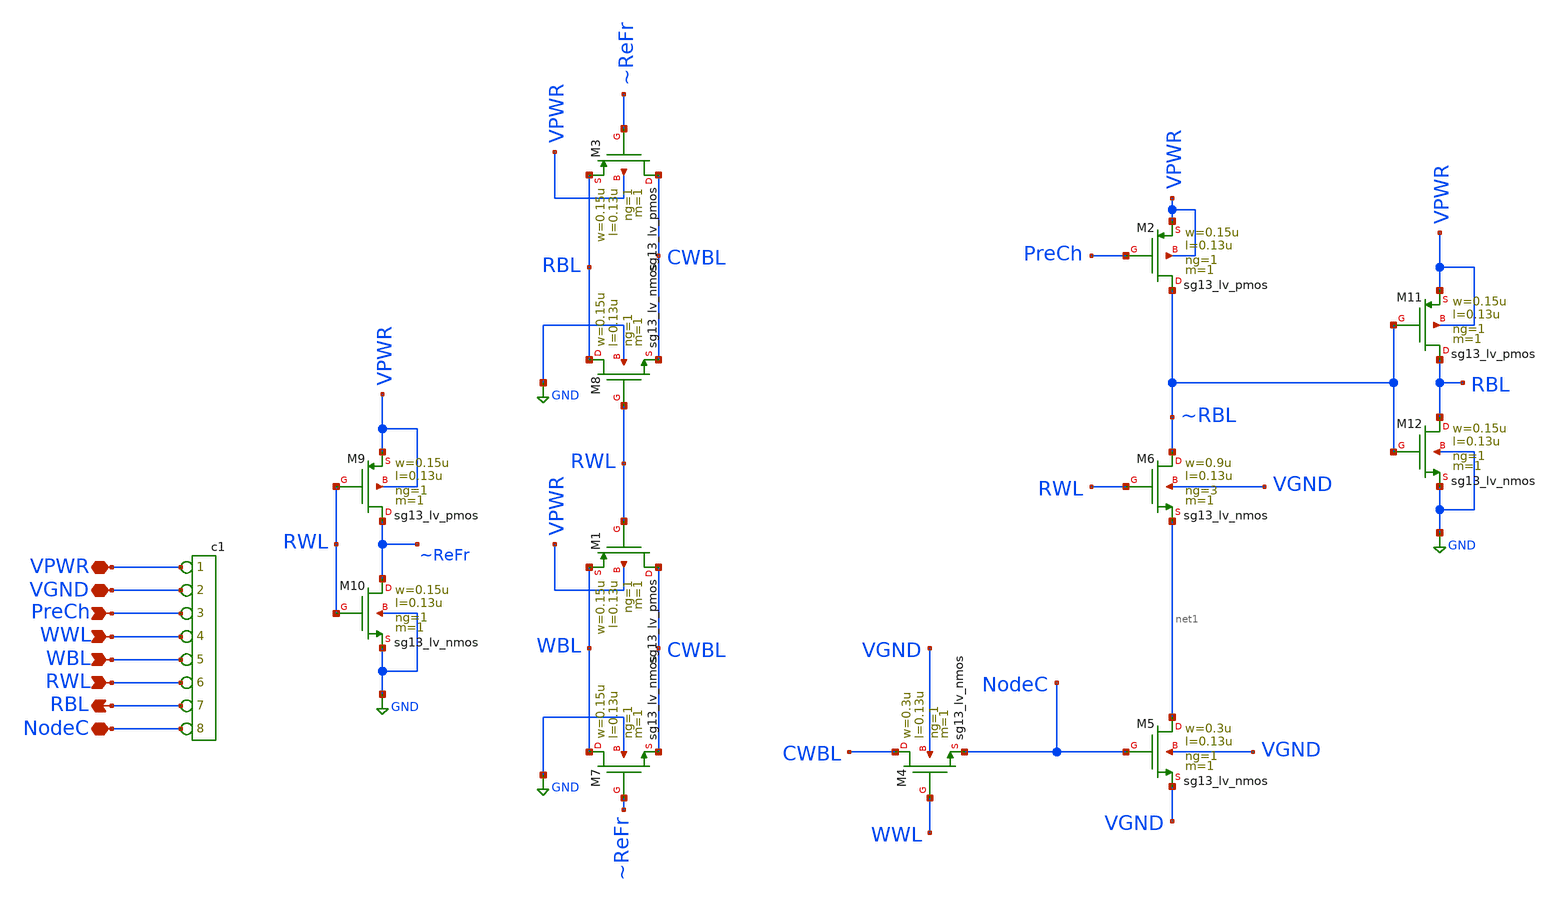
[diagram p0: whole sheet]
** sch_path: macros/heichips26_analog_project/macros/dramcell_2_0/schematic/xschem/untitled.sch
**.subckt untitled RBL WWL WBL RWL VGND NodeC VPWR PreCh
*.opin RBL
*.ipin WWL
*.ipin WBL
*.ipin RWL
*.iopin VGND
*.iopin NodeC
*.iopin VPWR
*.ipin PreCh
XM4 CWBL WWL NodeC VGND sg13_lv_nmos w=0.3u l=0.13u ng=1 m=1 mm_ok=1
XM5 net1 NodeC VGND VGND sg13_lv_nmos w=0.3u l=0.13u ng=1 m=1 mm_ok=1
XM6 ~RBL RWL net1 VGND sg13_lv_nmos w=0.9u l=0.13u ng=3 m=1 mm_ok=1
XM2 ~RBL PreCh VPWR VPWR sg13_lv_pmos w=0.15u l=0.13u ng=1 m=1 mm_ok=1
XM1 CWBL RWL WBL VPWR sg13_lv_pmos w=0.15u l=0.13u ng=1 m=1 mm_ok=1
XM7 WBL ~ReFr CWBL GND sg13_lv_nmos w=0.15u l=0.13u ng=1 m=1 mm_ok=1
XM3 CWBL ~ReFr RBL VPWR sg13_lv_pmos w=0.15u l=0.13u ng=1 m=1 mm_ok=1
XM8 RBL RWL CWBL GND sg13_lv_nmos w=0.15u l=0.13u ng=1 m=1 mm_ok=1
XM9 ~ReFr RWL VPWR VPWR sg13_lv_pmos w=0.15u l=0.13u ng=1 m=1 mm_ok=1
XM10 ~ReFr RWL GND GND sg13_lv_nmos w=0.15u l=0.13u ng=1 m=1 mm_ok=1
XM11 RBL ~RBL VPWR VPWR sg13_lv_pmos w=0.15u l=0.13u ng=1 m=1 mm_ok=1
XM12 RBL ~RBL GND GND sg13_lv_nmos w=0.15u l=0.13u ng=1 m=1 mm_ok=1
*connector(8,1) ?1 VPWR ?1 VGND ?1 PreCh ?1 WWL ?1 WBL ?1 RWL ?1 RBL ?1 NodeC
**.ends
.GLOBAL GND
.end
